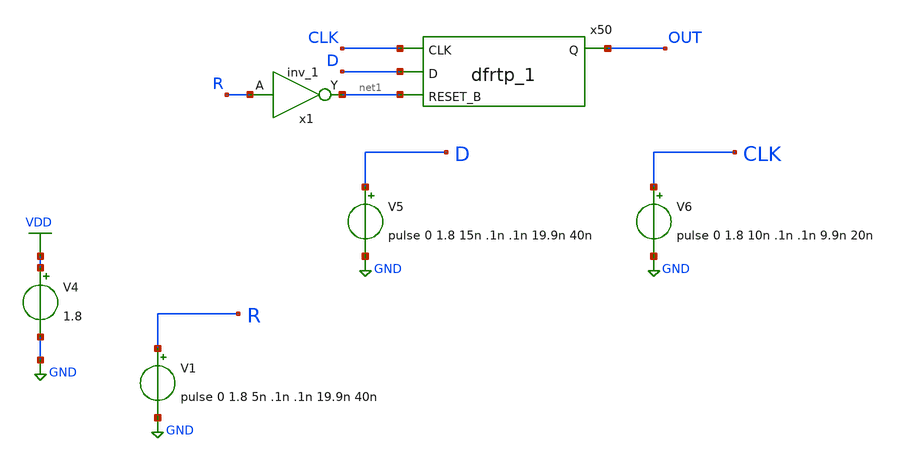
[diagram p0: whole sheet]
** sch_path: tb_df.sch
**.subckt tb_df
x50 CLK D net1 GND GND VDD VDD OUT sky130_fd_sc_hd__dfrtp_1
V4 VDD GND 1.8
V5 D GND pulse 0 1.8 15n .1n .1n 19.9n 40n
V6 CLK GND pulse 0 1.8 10n .1n .1n 9.9n 20n
V1 R GND pulse 0 1.8 5n .1n .1n 19.9n 40n
x1 R GND GND VDD VDD net1 sky130_fd_sc_hd__inv_1
**** begin user architecture code
 .lib $::SKYWATER_MODELS/sky130.lib.spice tt
.include $::SKYWATER_STDCELLS/sky130_fd_sc_hd.spice



.options acct list
.temp 25

.tran 1n 0.1u
.control
.write tb_saradc.raw
.endc


**** end user architecture code
**.ends
.GLOBAL VDD
.GLOBAL GND
.end
